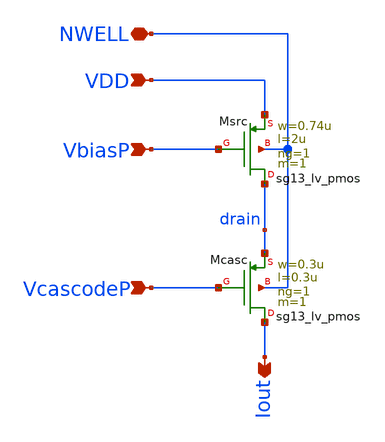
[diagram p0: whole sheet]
** sch_path: xschem/pcascsrc.sch
**.subckt pcascsrc VcascodeP VbiasP Iout VDD NWELL
*.ipin VcascodeP
*.ipin VbiasP
*.opin Iout
*.ipin VDD
*.iopin NWELL
XMsrc drain VbiasP VDD NWELL sg13_lv_pmos w=0.74u l=2u ng=1 m=1 mm_ok=1
XMcasc Iout VcascodeP drain NWELL sg13_lv_pmos w=0.3u l=0.3u ng=1 m=1 mm_ok=1
**.ends
.end
